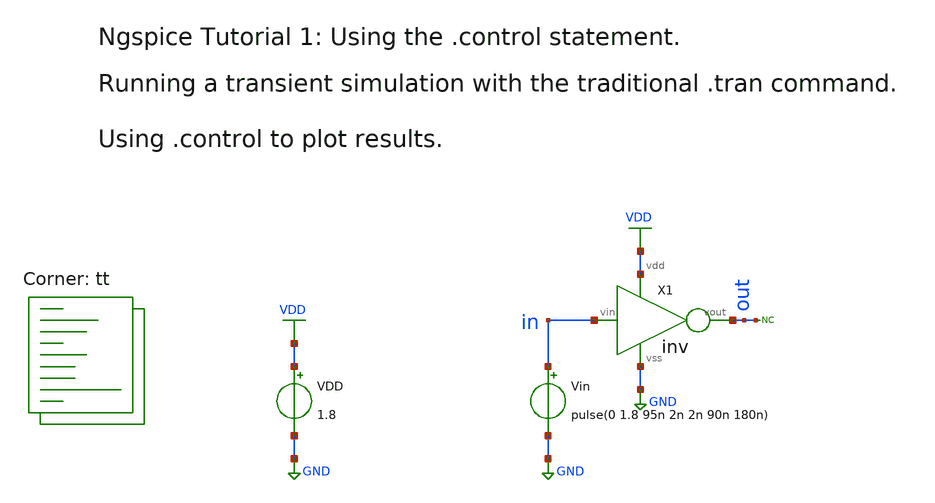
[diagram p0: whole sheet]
** sch_path: xsch/tut/ngspice_tut1.sch
**.subckt ngspice_tut1
Vin in GND pulse(0 1.8 95n 2n 2n 90n 180n)
VDD VDD GND 1.8
X1 in out VDD GND inv
* noconn out
**** begin user architecture code


.tran 100p 500n

* control language script

.control
run						; run the .tran command
set xbrushwidth=2						; set linewidth of the graph
plot v(in) v(out)						; plot the simulation results

.endc
.end



.lib $::SKYWATER_MODELS/sky130.lib.spice tt
**** end user architecture code
**.ends
.GLOBAL VDD
.GLOBAL GND
.end
